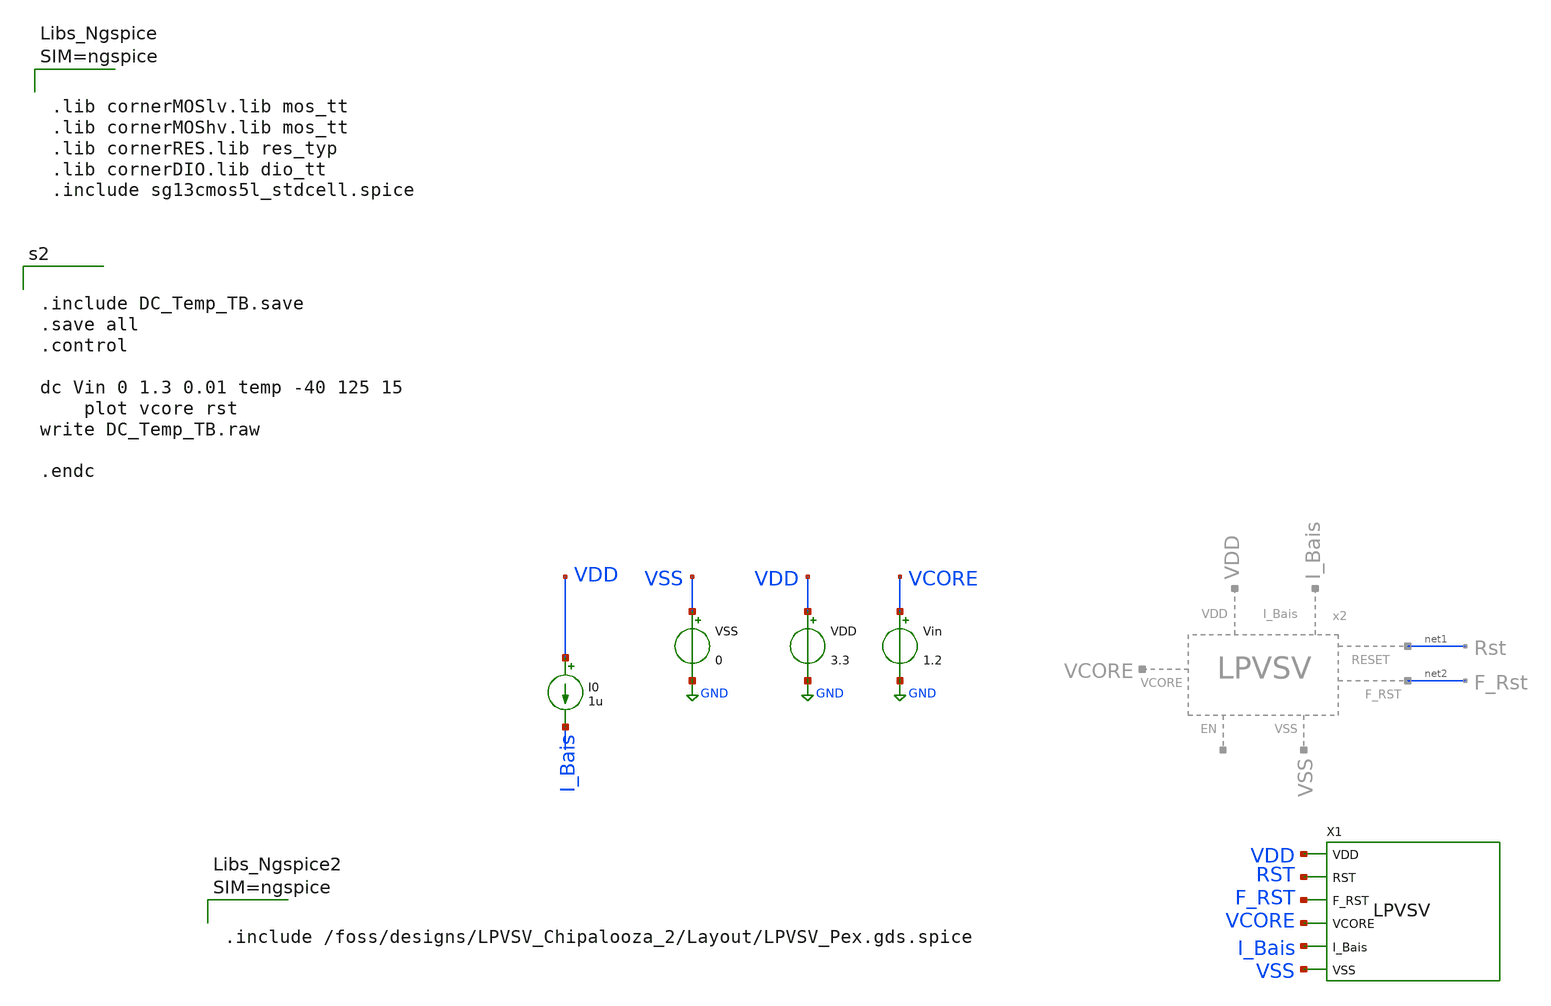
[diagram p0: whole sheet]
** sch_path: Simulation/DC_Temp_TB.sch
**.subckt DC_Temp_TB
VDD VDD GND 3.3
VSS VSS GND 0
Vin VCORE GND 1.2
I0 VDD I_Bais 1u
X1 VSS F_RST VDD VCORE I_Bais RST LPVSV
**** begin user architecture code


.include DC_Temp_TB.save
.save all
.control

dc Vin 0 1.3 0.01 temp -40 125 15
	plot vcore rst
write DC_Temp_TB.raw

.endc




.options rshunt = 1e15
.options gmin=1e-9
.options reltol = 0.01 abstol = 1p
.option filetype=ascii





.lib cornerMOSlv.lib mos_tt
.lib cornerMOShv.lib mos_tt
.lib cornerRES.lib res_typ
.lib cornerDIO.lib dio_tt
.include sg13cmos5l_stdcell.spice






.include /foss/designs/LPVSV_Chipalooza_2/Layout/LPVSV_Pex.gds.spice



**** end user architecture code
**.ends
.GLOBAL GND
.end
